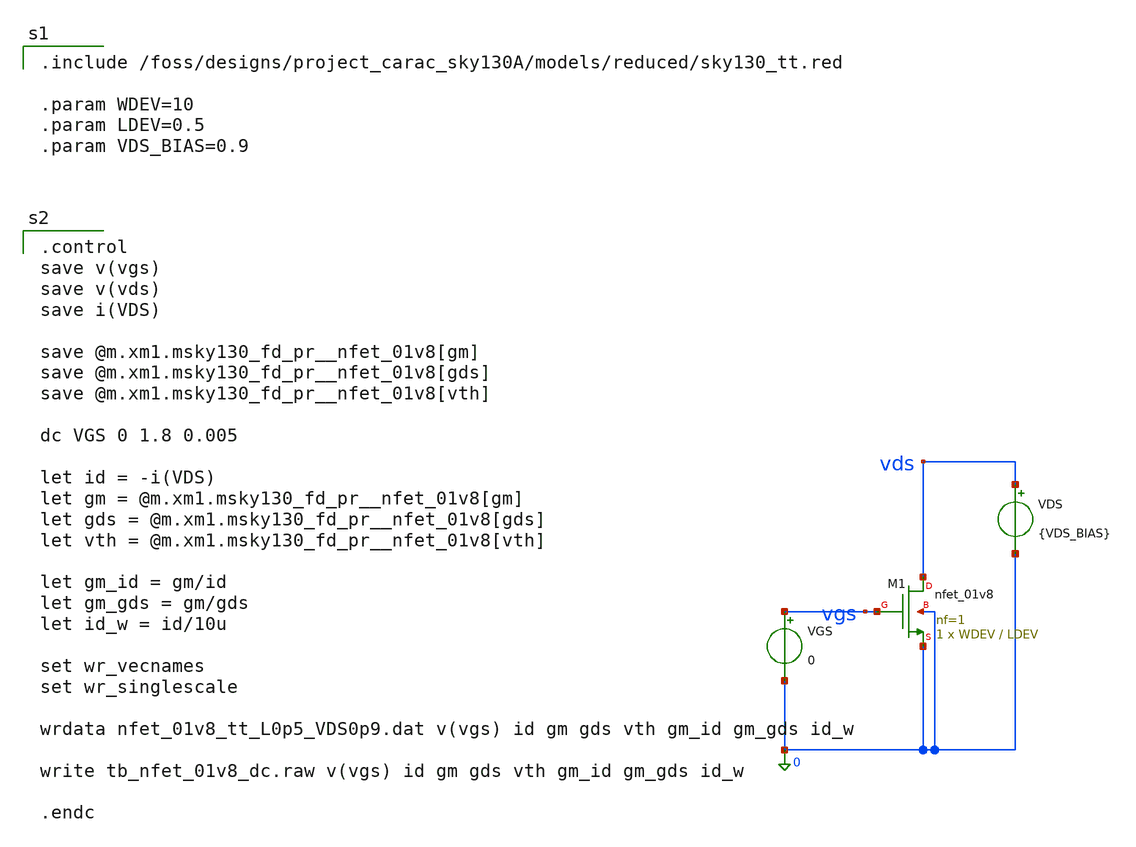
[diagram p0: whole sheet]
** sch_path: dfii/project_carac_sky130A_sim/tb_nfet_01v8_dc.sch
* Copyright 2021 Stefan Frederik Schippers
* Licensed under the Apache License, Version 2.0 (the "License");
* you may not use this file except in compliance with the License.
* You may obtain a copy of the License at
* https://www.apache.org/licenses/LICENSE-2.0
* Unless required by applicable law or agreed to in writing, software
* distributed under the License is distributed on an "AS IS" BASIS,
* WITHOUT WARRANTIES OR CONDITIONS OF ANY KIND, either express or implied.
* See the License for the specific language governing permissions and
* limitations under the License.

.include /foss/designs/project_carac_sky130A/models/reduced/sky130_tt.red

.param WDEV=10
.param LDEV=0.5
.param VDS_BIAS=0.9



**.subckt tb_nfet_01v8_dc
XM1 vds vgs 0 0 sky130_fd_pr__nfet_01v8 L=LDEV W=WDEV nf=1 ad='int((1 + 1)/2) * WDEV / 1 * 0.29' as='int((1 + 2)/2) * WDEV / 1 * 0.29'
+ pd='2*int((1 + 1)/2) * (WDEV / 1 + 0.29)' ps='2*int((1 + 2)/2) * (WDEV / 1 + 0.29)' nrd='0.29 / WDEV '
+ nrs='0.29 / WDEV ' sa=0 sb=0 sd=0 mult=1 m=1
VGS vgs 0 0
VDS vds 0 {VDS_BIAS}
**.ends
**** begin user architecture code

.control
save v(vgs)
save v(vds)
save i(VDS)

save @m.xm1.msky130_fd_pr__nfet_01v8[gm]
save @m.xm1.msky130_fd_pr__nfet_01v8[gds]
save @m.xm1.msky130_fd_pr__nfet_01v8[vth]

dc VGS 0 1.8 0.005

let id = -i(VDS)
let gm = @m.xm1.msky130_fd_pr__nfet_01v8[gm]
let gds = @m.xm1.msky130_fd_pr__nfet_01v8[gds]
let vth = @m.xm1.msky130_fd_pr__nfet_01v8[vth]

let gm_id = gm/id
let gm_gds = gm/gds
let id_w = id/10u

set wr_vecnames
set wr_singlescale

wrdata nfet_01v8_tt_L0p5_VDS0p9.dat v(vgs) id gm gds vth gm_id gm_gds id_w

write tb_nfet_01v8_dc.raw v(vgs) id gm gds vth gm_id gm_gds id_w

.endc

**** end user architecture code
.end
